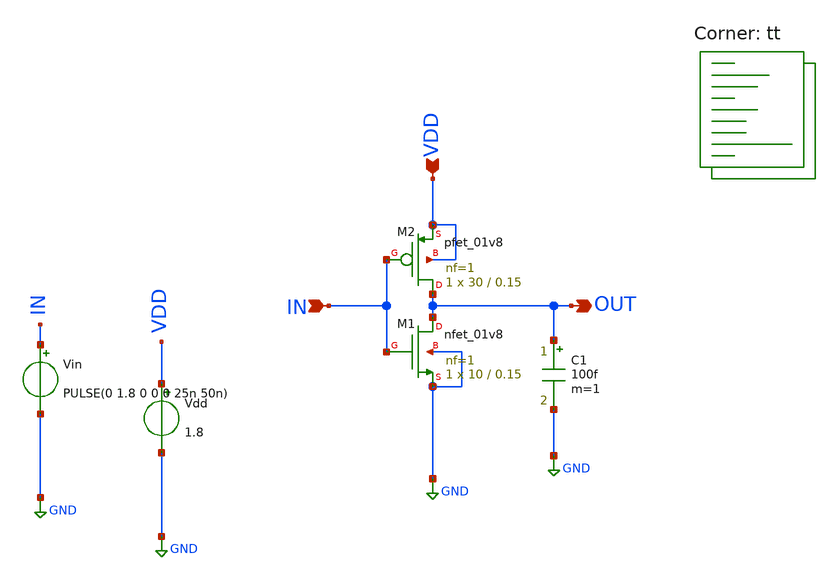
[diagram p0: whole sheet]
** sch_path: sizing-inverter.sch
**.subckt sizing-inverter IN VDD OUT
*.ipin IN
*.ipin VDD
*.opin OUT
Vin IN GND PULSE(0 1.8 0 0 0 25n 50n)
Vdd VDD GND 1.8
XM1 OUT IN GND GND sky130_fd_pr__nfet_01v8 L=0.15 W=10 nf=1 ad='int((nf+1)/2) * W/nf * 0.29' as='int((nf+2)/2) * W/nf * 0.29'
+ pd='2*int((nf+1)/2) * (W/nf + 0.29)' ps='2*int((nf+2)/2) * (W/nf + 0.29)' nrd='0.29 / W' nrs='0.29 / W'
+ sa=0 sb=0 sd=0 mult=1 m=1
XM2 OUT IN VDD VDD sky130_fd_pr__pfet_01v8 L=0.15 W=30 nf=1 ad='int((nf+1)/2) * W/nf * 0.29' as='int((nf+2)/2) * W/nf * 0.29'
+ pd='2*int((nf+1)/2) * (W/nf + 0.29)' ps='2*int((nf+2)/2) * (W/nf + 0.29)' nrd='0.29 / W' nrs='0.29 / W'
+ sa=0 sb=0 sd=0 mult=1 m=1
C1 OUT GND 100f m=1
**** begin user architecture code
.lib $::SKYWATER_MODELS/sky130.lib.spice tt


*.options savecurrents

.control
let step_nmos=10
let step_pmos=1

let index_nmos=0
let index_pmos= 0

let final_w_nmos=30
let final_w_pmos=80

let current_w_nmos=20

let total_iterations_nmos = ceil((final_w_nmos - current_w_nmos)/step_nmos)
let total_iterations_pmos = ceil((final_w_pmos - current_w_pmos)/step_pmos)

let net_swiching_points = vector(total_iterations_nmos)
let net_asymmetricity = vector(total_iterations_nmos)
let width_nmos = vector(total_iterations_nmos)


let switching_points = vector(total_iterations_pmos)
let asymmetricity = vector(total_iterations_pmos)
let width_pmos = vector(total_iterations_pmos)


***** Start varying nmos widths ****
while current_w_nmos <= final_w_nmos
  let current_w_pmos=10

  alter m.xm1.msky130_fd_pr__nfet_01v8 W=current_w_nmos

**** Start varying pmos widths ******
  while current_w_pmos < final_w_pmos

    alter m.xm2.msky130_fd_pr__pfet_01v8 W=current_w_pmos

******* Asymmetricity simulation with pulse of 50n with 1/2 duty cycle ********
    tran 10p 50n

    meas tran rise_time TRIG v(out) VAL=0.1 RISE=1 TARG v(out) VAL=1.62 RISE=1
    meas tran fall_time TRIG v(out) VAL=1.62 FALL=1 TARG v(out) VAL=0.1 FALL=1

    let asymmetricity[index_pmos] = abs( $&rise_time - $&fall_time )



******* Switching point simulation ********
    dc vin 0 1.8 1m

    meas dc switching_point WHEN v(out)=v(in) CROSS=LAST

    let switching_points[index_pmos] = $&switching_point
    let width_pmos[index_pmos] = current_w_pmos

    let current_w_pmos=current_w_pmos + step_pmos
    let index_pmos=index_pmos + 1

  end

**** Stop varying pmos widths ******



******* Find switching point at most symmetric w (this is per nmos iteration) ********
  let lowest_asym = 100
  let best_w_index = 0
  let iterate_pmos = 0
  let tolerance = 1p
 * We let the asymmetricity be plus/minus 1p of 0

  repeat $&total_iterations_pmos

    let asym = abs(asymmetricity[iterate_pmos] - 1p)
    let current_w_pmos = width_pmos[iterate_pmos]

    if asym < lowest_asym
      let best_w_index = iterate_pmos
      let lowest_asym = asym
    end

    let iterate_pmos = iterate_pmos + 1
  end

* Now that we have the best width, we now need to move towards getting the switching point

* Select the cream of the crop
  let net_switching_points[index_nmos] = switching_points[best_w_index]
  let net_asymmetricity[index_nmos] = asymmetricity[best_w_index]

* Associate it to the nmos value
  let width_nmos[index_nmos] = current_w_nmos



  let index_nmos = index_nmos + 1
  let current_w_nmos = current_w_nmos + step_nmos

end

**** Stop varying nmos widths ****

set nolegend

******* Plot results ********
plot net_switching_points vs width_nmos
plot net_asymmetricity vs width_nmos
.endc




*.options savecurrents

.control
let step_nmos=1
let step_pmos=1

let index_nmos=0
let index_pmos= 0

let final_w_nmos=13
let final_w_pmos=60

let current_w_nmos=10

let total_iterations_nmos = ceil((final_w_nmos - current_w_nmos)/step_nmos)
let total_iterations_pmos = ceil((final_w_pmos - current_w_pmos)/step_pmos)

let net_swiching_points = vector(total_iterations_nmos)
let net_asymmetricity = vector(total_iterations_nmos)
let width_nmos = vector(total_iterations_nmos)


let switching_points = vector(total_iterations_pmos)
let asymmetricity = vector(total_iterations_pmos)
let width_pmos = vector(total_iterations_pmos)


***** Start varying nmos widths ****
while current_w_nmos <= final_w_nmos
  let current_w_pmos=10

  alter m.xm1.msky130_fd_pr__nfet_01v8 W=current_w_nmos

**** Start varying pmos widths ******
  while current_w_pmos < final_w_pmos

    alter m.xm2.msky130_fd_pr__pfet_01v8 W=current_w_pmos

******* Asymmetricity simulation with pulse of 50n with 1/2 duty cycle ********
    tran 10p 50n

    meas tran rise_time TRIG v(out) VAL=0.1 RISE=1 TARG v(out) VAL=1.62 RISE=1
    meas tran fall_time TRIG v(out) VAL=1.62 FALL=1 TARG v(out) VAL=0.1 FALL=1

    let asymmetricity[index_pmos] = abs( $&rise_time - $&fall_time )



******* Switching point simulation ********
    dc vin 0 1.8 1m

    meas dc switching_point WHEN v(out)=v(in) CROSS=LAST

    let switching_points[index_pmos] = $&switching_point
    let width_pmos[index_pmos] = current_w_pmos

    let current_w_pmos=current_w_pmos + step_pmos
    let index_pmos=index_pmos + 1

  end

**** Stop varying pmos widths ******



******* Find switching point at most symmetric w (this is per nmos iteration) ********
  let lowest_asym = 100
  let best_w_index = 0
  let iterate_pmos = 0
  let tolerance = 1p
 * We let the asymmetricity be plus/minus 1p of 0

  repeat $&total_iterations_pmos

    let asym = abs(asymmetricity[iterate_pmos] - 1p)
    let current_w_pmos = width_pmos[iterate_pmos]

    if asym < lowest_asym
      let best_w_index = iterate_pmos
      let lowest_asym = asym
    end

    let iterate_pmos = iterate_pmos + 1
  end

* Now that we have the best width, we now need to move towards getting the switching point

* Select the cream of the crop
  let net_switching_points[index_nmos] = switching_points[best_w_index]
  let net_asymmetricity[index_nmos] = asymmetricity[best_w_index]

* Associate it to the nmos value
  let width_nmos[index_nmos] = current_w_nmos



  let index_nmos = index_nmos + 1
  let current_w_nmos = current_w_nmos + step_nmos

end

**** Stop varying nmos widths ****

set nolegend

******* Plot results ********
plot net_switching_points vs width_nmos
plot net_asymmetricity vs width_nmos
.endc


**** end user architecture code
**.ends
.GLOBAL GND
.end
